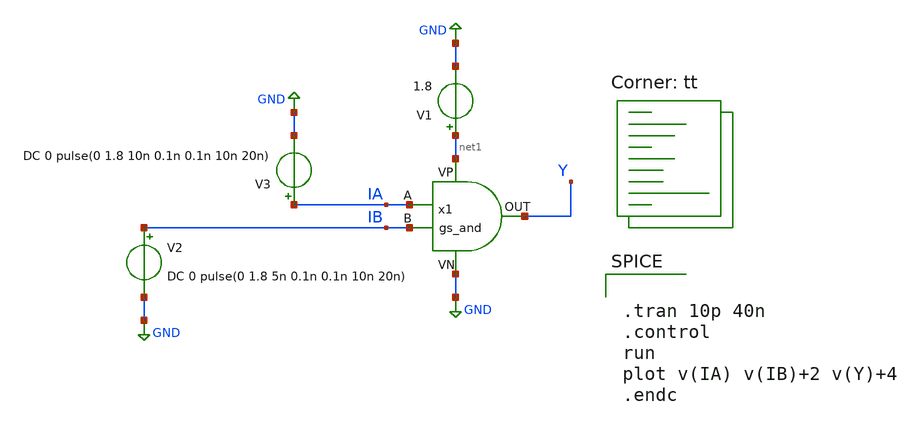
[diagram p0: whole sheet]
** sch_path: APIC-3/schematic/and_gate/tb_gs_and.sch
**.subckt tb_gs_and
V1 net1 GND 1.8
V2 IB GND DC 0 pulse(0 1.8 5n 0.1n 0.1n 10n 20n)
V3 IA GND DC 0 pulse(0 1.8 10n 0.1n 0.1n 10n 20n)
x1 IA IB Y net1 GND gs_and
**** begin user architecture code


.tran 10p 40n
.control
run
plot v(IA) v(IB)+2 v(Y)+4
.endc


.lib $::SKYWATER_MODELS/sky130.lib.spice tt
**** end user architecture code
**.ends
.GLOBAL GND
.end
